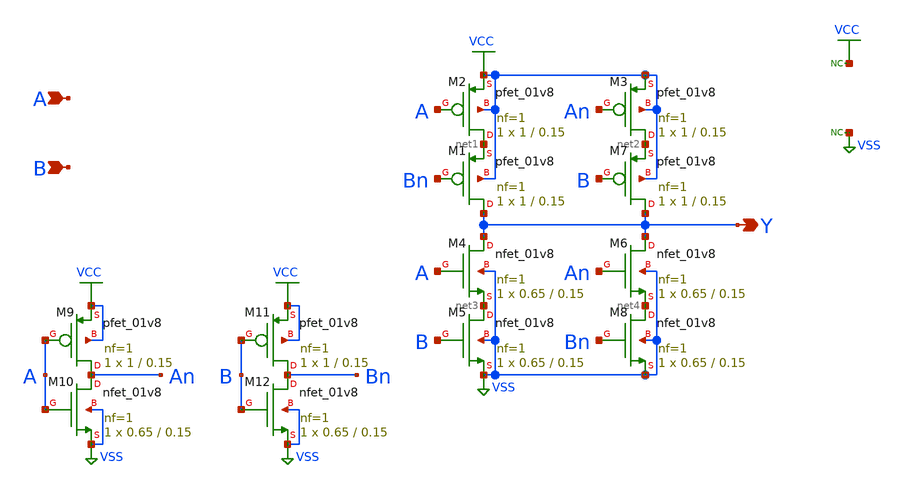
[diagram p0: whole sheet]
** sch_path: elements/xor.sch
**.subckt xor A B Y
*.ipin A
*.ipin B
*.opin Y
* noconn VCC
* noconn VSS
XM2 net1 A VCC VCC sky130_fd_pr__pfet_01v8 L=0.15 W=1 nf=1 ad='int((nf+1)/2) * W/nf * 0.29' as='int((nf+2)/2) * W/nf * 0.29'
+ pd='2*int((nf+1)/2) * (W/nf + 0.29)' ps='2*int((nf+2)/2) * (W/nf + 0.29)' nrd='0.29 / W' nrs='0.29 / W'
+ sa=0 sb=0 sd=0 mult=1 m=1
XM1 Y Bn net1 VCC sky130_fd_pr__pfet_01v8 L=0.15 W=1 nf=1 ad='int((nf+1)/2) * W/nf * 0.29' as='int((nf+2)/2) * W/nf * 0.29'
+ pd='2*int((nf+1)/2) * (W/nf + 0.29)' ps='2*int((nf+2)/2) * (W/nf + 0.29)' nrd='0.29 / W' nrs='0.29 / W'
+ sa=0 sb=0 sd=0 mult=1 m=1
XM3 net2 An VCC VCC sky130_fd_pr__pfet_01v8 L=0.15 W=1 nf=1 ad='int((nf+1)/2) * W/nf * 0.29' as='int((nf+2)/2) * W/nf * 0.29'
+ pd='2*int((nf+1)/2) * (W/nf + 0.29)' ps='2*int((nf+2)/2) * (W/nf + 0.29)' nrd='0.29 / W' nrs='0.29 / W'
+ sa=0 sb=0 sd=0 mult=1 m=1
XM4 Y A net3 VSS sky130_fd_pr__nfet_01v8 L=0.15 W=0.65 nf=1 ad='int((1 + 1)/2) * 0.65 / 1 * 0.29' as='int((1 + 2)/2) * 0.65 / 1 * 0.29'
+ pd='2*int((1 + 1)/2) * (0.65 / 1 + 0.29)' ps='2*int((1 + 2)/2) * (0.65 / 1 + 0.29)' nrd='0.29 / 0.65 '
+ nrs='0.29 / 0.65 ' sa=0 sb=0 sd=0 mult=1 m=1
XM5 net3 B VSS VSS sky130_fd_pr__nfet_01v8 L=0.15 W=0.65 nf=1 ad='int((1 + 1)/2) * 0.65 / 1 * 0.29' as='int((1 + 2)/2) * 0.65 / 1 * 0.29'
+ pd='2*int((1 + 1)/2) * (0.65 / 1 + 0.29)' ps='2*int((1 + 2)/2) * (0.65 / 1 + 0.29)' nrd='0.29 / 0.65 '
+ nrs='0.29 / 0.65 ' sa=0 sb=0 sd=0 mult=1 m=1
XM6 Y An net4 VSS sky130_fd_pr__nfet_01v8 L=0.15 W=0.65 nf=1 ad='int((1 + 1)/2) * 0.65 / 1 * 0.29' as='int((1 + 2)/2) * 0.65 / 1 * 0.29'
+ pd='2*int((1 + 1)/2) * (0.65 / 1 + 0.29)' ps='2*int((1 + 2)/2) * (0.65 / 1 + 0.29)' nrd='0.29 / 0.65 '
+ nrs='0.29 / 0.65 ' sa=0 sb=0 sd=0 mult=1 m=1
XM7 Y B net2 VCC sky130_fd_pr__pfet_01v8 L=0.15 W=1 nf=1 ad='int((nf+1)/2) * W/nf * 0.29' as='int((nf+2)/2) * W/nf * 0.29'
+ pd='2*int((nf+1)/2) * (W/nf + 0.29)' ps='2*int((nf+2)/2) * (W/nf + 0.29)' nrd='0.29 / W' nrs='0.29 / W'
+ sa=0 sb=0 sd=0 mult=1 m=1
XM8 net4 Bn VSS VSS sky130_fd_pr__nfet_01v8 L=0.15 W=0.65 nf=1 ad='int((1 + 1)/2) * 0.65 / 1 * 0.29'
+ as='int((1 + 2)/2) * 0.65 / 1 * 0.29' pd='2*int((1 + 1)/2) * (0.65 / 1 + 0.29)' ps='2*int((1 + 2)/2) * (0.65 / 1 + 0.29)'
+ nrd='0.29 / 0.65 ' nrs='0.29 / 0.65 ' sa=0 sb=0 sd=0 mult=1 m=1
XM9 An A VCC VCC sky130_fd_pr__pfet_01v8 L=0.15 W=1 nf=1 ad='int((nf+1)/2) * W/nf * 0.29' as='int((nf+2)/2) * W/nf * 0.29'
+ pd='2*int((nf+1)/2) * (W/nf + 0.29)' ps='2*int((nf+2)/2) * (W/nf + 0.29)' nrd='0.29 / W' nrs='0.29 / W'
+ sa=0 sb=0 sd=0 mult=1 m=1
XM10 An A VSS VSS sky130_fd_pr__nfet_01v8 L=0.15 W=0.65 nf=1 ad='int((1 + 1)/2) * 0.65 / 1 * 0.29' as='int((1 + 2)/2) * 0.65 / 1 * 0.29'
+ pd='2*int((1 + 1)/2) * (0.65 / 1 + 0.29)' ps='2*int((1 + 2)/2) * (0.65 / 1 + 0.29)' nrd='0.29 / 0.65 '
+ nrs='0.29 / 0.65 ' sa=0 sb=0 sd=0 mult=1 m=1
XM11 Bn B VCC VCC sky130_fd_pr__pfet_01v8 L=0.15 W=1 nf=1 ad='int((nf+1)/2) * W/nf * 0.29' as='int((nf+2)/2) * W/nf * 0.29'
+ pd='2*int((nf+1)/2) * (W/nf + 0.29)' ps='2*int((nf+2)/2) * (W/nf + 0.29)' nrd='0.29 / W' nrs='0.29 / W'
+ sa=0 sb=0 sd=0 mult=1 m=1
XM12 Bn B VSS VSS sky130_fd_pr__nfet_01v8 L=0.15 W=0.65 nf=1 ad='int((1 + 1)/2) * 0.65 / 1 * 0.29' as='int((1 + 2)/2) * 0.65 / 1 * 0.29'
+ pd='2*int((1 + 1)/2) * (0.65 / 1 + 0.29)' ps='2*int((1 + 2)/2) * (0.65 / 1 + 0.29)' nrd='0.29 / 0.65 '
+ nrs='0.29 / 0.65 ' sa=0 sb=0 sd=0 mult=1 m=1
**.ends
.GLOBAL VCC
.GLOBAL VSS
.end
